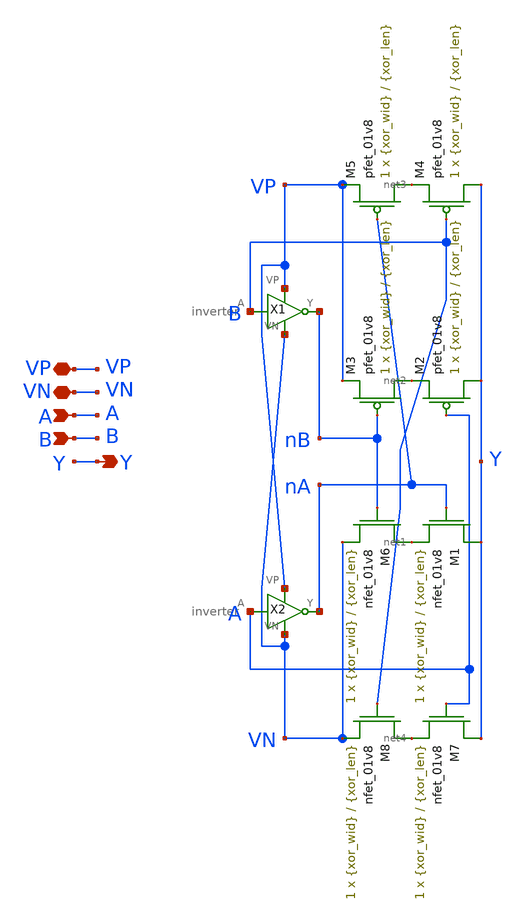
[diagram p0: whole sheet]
** sch_path: LDS/LDS_xor.sch
**.subckt LDS_xor VN VP Y A B
*.iopin VN
*.iopin VP
*.opin Y
*.ipin A
*.ipin B
X2 A nA VP VN inverter
X1 B nB VP VN inverter
XM1 Y nA net1 VN sky130_fd_pr__nfet_01v8 L={xor_len} W={xor_wid} nf=1 ad='int((nf+1)/2) * W/nf * 0.29'
+ as='int((nf+2)/2) * W/nf * 0.29' pd='2*int((nf+1)/2) * (W/nf + 0.29)' ps='2*int((nf+2)/2) * (W/nf + 0.29)'
+ nrd='0.29 / W' nrs='0.29 / W' sa=0 sb=0 sd=0 mult=1 m=1
XM2 Y A net2 VP sky130_fd_pr__pfet_01v8 L={xor_len} W={xor_wid} nf=1 ad='int((nf+1)/2) * W/nf * 0.29'
+ as='int((nf+2)/2) * W/nf * 0.29' pd='2*int((nf+1)/2) * (W/nf + 0.29)' ps='2*int((nf+2)/2) * (W/nf + 0.29)'
+ nrd='0.29 / W' nrs='0.29 / W' sa=0 sb=0 sd=0 mult=1 m=1
XM3 net2 nB VP VP sky130_fd_pr__pfet_01v8 L={xor_len} W={xor_wid} nf=1 ad='int((nf+1)/2) * W/nf * 0.29'
+ as='int((nf+2)/2) * W/nf * 0.29' pd='2*int((nf+1)/2) * (W/nf + 0.29)' ps='2*int((nf+2)/2) * (W/nf + 0.29)'
+ nrd='0.29 / W' nrs='0.29 / W' sa=0 sb=0 sd=0 mult=1 m=1
XM4 Y B net3 VP sky130_fd_pr__pfet_01v8 L={xor_len} W={xor_wid} nf=1 ad='int((nf+1)/2) * W/nf * 0.29'
+ as='int((nf+2)/2) * W/nf * 0.29' pd='2*int((nf+1)/2) * (W/nf + 0.29)' ps='2*int((nf+2)/2) * (W/nf + 0.29)'
+ nrd='0.29 / W' nrs='0.29 / W' sa=0 sb=0 sd=0 mult=1 m=1
XM5 net3 nA VP VP sky130_fd_pr__pfet_01v8 L={xor_len} W={xor_wid} nf=1 ad='int((nf+1)/2) * W/nf * 0.29'
+ as='int((nf+2)/2) * W/nf * 0.29' pd='2*int((nf+1)/2) * (W/nf + 0.29)' ps='2*int((nf+2)/2) * (W/nf + 0.29)'
+ nrd='0.29 / W' nrs='0.29 / W' sa=0 sb=0 sd=0 mult=1 m=1
XM6 net1 nB VN VN sky130_fd_pr__nfet_01v8 L={xor_len} W={xor_wid} nf=1 ad='int((nf+1)/2) * W/nf * 0.29'
+ as='int((nf+2)/2) * W/nf * 0.29' pd='2*int((nf+1)/2) * (W/nf + 0.29)' ps='2*int((nf+2)/2) * (W/nf + 0.29)'
+ nrd='0.29 / W' nrs='0.29 / W' sa=0 sb=0 sd=0 mult=1 m=1
XM7 Y A net4 VN sky130_fd_pr__nfet_01v8 L={xor_len} W={xor_wid} nf=1 ad='int((nf+1)/2) * W/nf * 0.29'
+ as='int((nf+2)/2) * W/nf * 0.29' pd='2*int((nf+1)/2) * (W/nf + 0.29)' ps='2*int((nf+2)/2) * (W/nf + 0.29)'
+ nrd='0.29 / W' nrs='0.29 / W' sa=0 sb=0 sd=0 mult=1 m=1
XM8 net4 B VN VN sky130_fd_pr__nfet_01v8 L={xor_len} W={xor_wid} nf=1 ad='int((nf+1)/2) * W/nf * 0.29'
+ as='int((nf+2)/2) * W/nf * 0.29' pd='2*int((nf+1)/2) * (W/nf + 0.29)' ps='2*int((nf+2)/2) * (W/nf + 0.29)'
+ nrd='0.29 / W' nrs='0.29 / W' sa=0 sb=0 sd=0 mult=1 m=1
**.ends

* expanding   symbol:  inverter.sym # of pins=4
** sym_path: LDS/inverter.sym
** sch_path: LDS/inverter.sch
.subckt inverter A Y VP VN
*.iopin VP
*.ipin A
*.opin Y
*.iopin VN
XM2 Y A VP VP sky130_fd_pr__pfet_01v8 L={inv_len} W={inv_wid} nf=1 ad='int((nf+1)/2) * W/nf * 0.29' as='int((nf+2)/2) * W/nf * 0.29'
+ pd='2*int((nf+1)/2) * (W/nf + 0.29)' ps='2*int((nf+2)/2) * (W/nf + 0.29)' nrd='0.29 / W' nrs='0.29 / W'
+ sa=0 sb=0 sd=0 mult=1 m=1
XM1 Y A VN VN sky130_fd_pr__nfet_01v8 L={inv_len} W={inv_wid} nf=1 ad='int((nf+1)/2) * W/nf * 0.29' as='int((nf+2)/2) * W/nf * 0.29'
+ pd='2*int((nf+1)/2) * (W/nf + 0.29)' ps='2*int((nf+2)/2) * (W/nf + 0.29)' nrd='0.29 / W' nrs='0.29 / W'
+ sa=0 sb=0 sd=0 mult=1 m=1
.ends

.end
